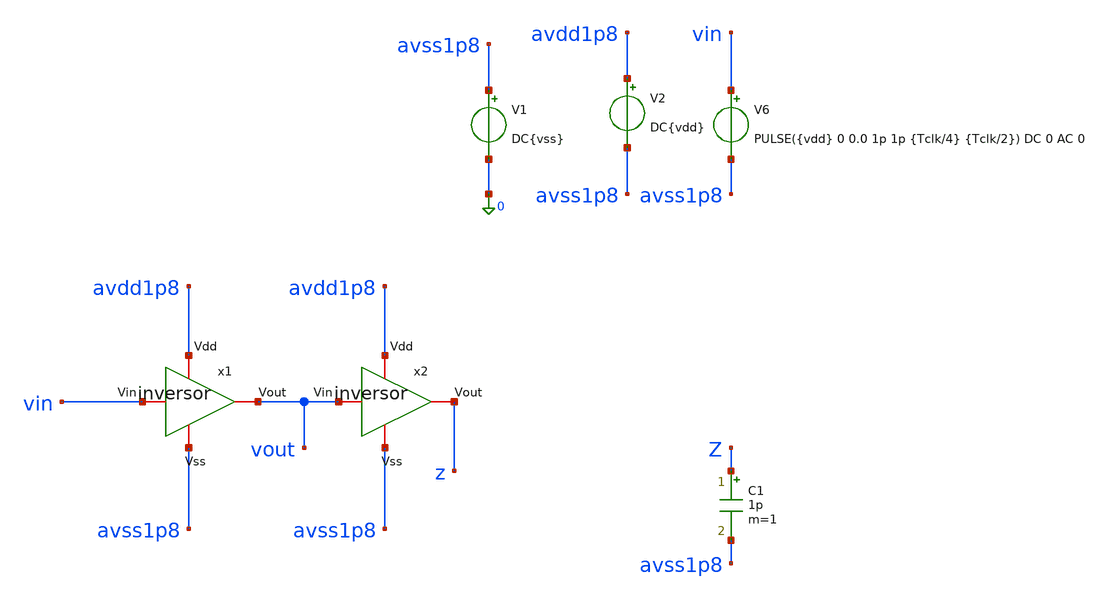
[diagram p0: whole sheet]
** sch_path: verification/testbenches/inversor/tb_inversor.sch
**.subckt tb_inversor
x1 avdd1p8 vout vin avss1p8 inversor
x2 avdd1p8 z vout avss1p8 inversor
V1 avss1p8 0 DC{vss}
V2 avdd1p8 avss1p8 DC{vdd}
V6 vin avss1p8 PULSE({vdd} 0 0.0 1p 1p {Tclk/4} {Tclk/2}) DC 0 AC 0
C1 Z avss1p8 1p m=1
**** begin user architecture code


* Circuit Parameters
.param vdd = 1.8
.param vss = 0.0
.param Tclk = 10n
.options TEMP = 65.0
* Include Models
.lib /foss/pdks/sky130A/libs.tech/ngspice/sky130.lib.spice TT
* OP Parameters & Singals to save
.save all
*Simulations
.control
tran 0.01u 100n
setplot tran1
plot v(vin) v(vout)+2
reset
dc V6 0 1.8 0.01
setplot dc
plot vin vout ylabel vout xlabel vin
set filetype = ascii
write dcsweep.raw
.endc
.end


**** end user architecture code
**.ends

* expanding   symbol:  blocks/inversor/schematic/inversor.sym # of pins=4
** sym_path: design/blocks/inversor/schematic/inversor.sym
** sch_path: design/blocks/inversor/schematic/inversor.sch
.subckt inversor Vdd Vout Vin Vss
*.iopin Vout
*.iopin Vin
*.iopin Vss
*.iopin Vdd
XM1 Vout Vin Vss Vss sg13_lv_nmos w=0.15u l=0.13u ng=1 m=1 mm_ok=1
XM2 Vout Vin Vdd Vdd sg13_lv_pmos w=0.15u l=0.13u ng=1 m=1 mm_ok=1
.ends

.end
